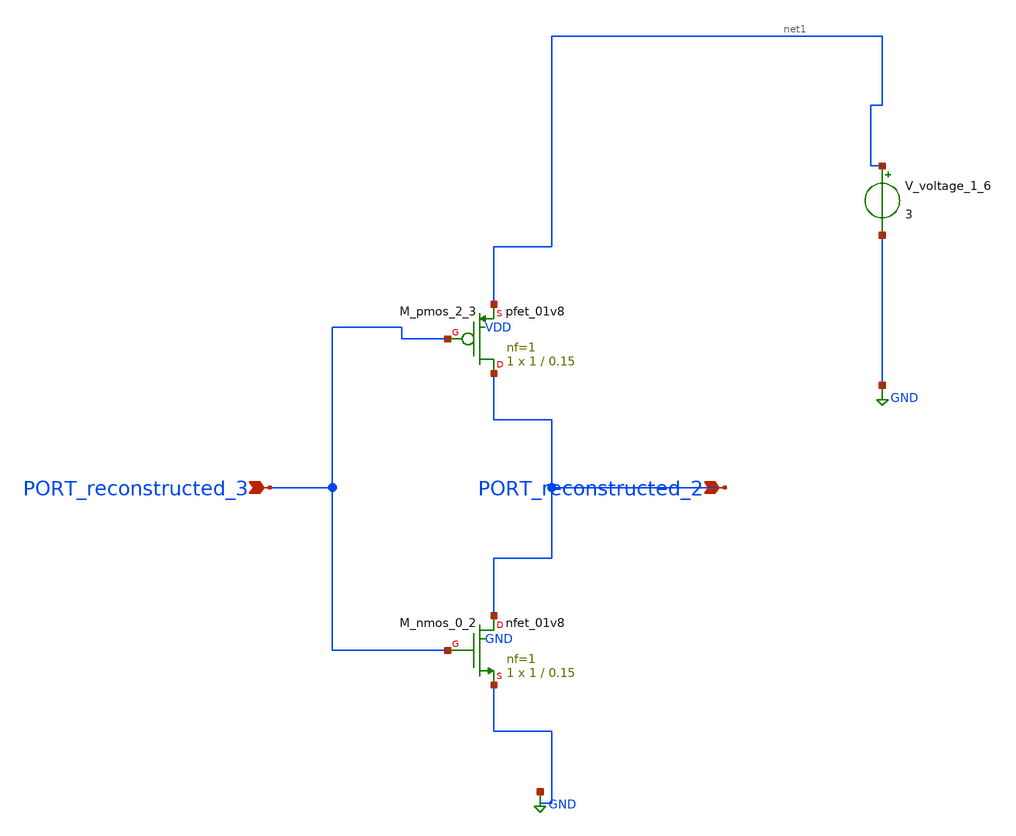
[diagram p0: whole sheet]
** sch_path: schematics/AMSNet/86.sch
**.subckt 86 PORT_reconstructed_2 PORT_reconstructed_3
*.ipin PORT_reconstructed_2
*.ipin PORT_reconstructed_3
XM_nmos_0_2 PORT_reconstructed_2 PORT_reconstructed_3 GND GND sky130_fd_pr__nfet_01v8 L=0.15 W=1 nf=1
+ ad='int((1 + 1)/2) * 1 / 1 * 0.29' as='int((1 + 2)/2) * 1 / 1 * 0.29' pd='2*int((1 + 1)/2) * (1 / 1 + 0.29)'
+ ps='2*int((1 + 2)/2) * (1 / 1 + 0.29)' nrd='0.29 / 1 ' nrs='0.29 / 1 ' sa=0 sb=0 sd=0 mult=1 m=1
XM_pmos_2_3 PORT_reconstructed_2 PORT_reconstructed_3 net1 VDD sky130_fd_pr__pfet_01v8 L=0.15 W=1 nf=1
+ ad='int((1 + 1)/2) * 1 / 1 * 0.29' as='int((1 + 2)/2) * 1 / 1 * 0.29' pd='2*int((1 + 1)/2) * (1 / 1 + 0.29)'
+ ps='2*int((1 + 2)/2) * (1 / 1 + 0.29)' nrd='0.29 / 1 ' nrs='0.29 / 1 ' sa=0 sb=0 sd=0 mult=1 m=1
V_voltage_1_6 net1 GND 3
**.ends
.GLOBAL GND
.end
